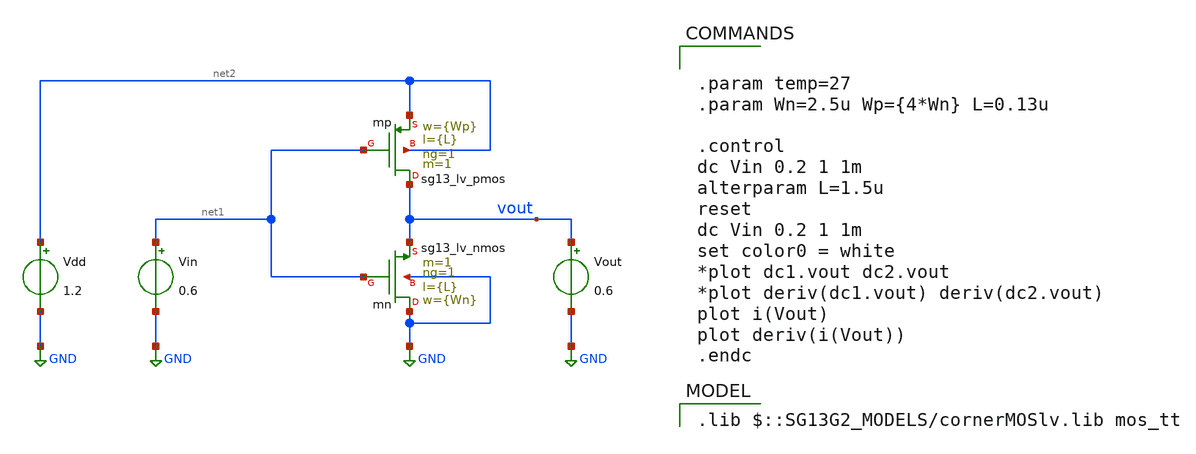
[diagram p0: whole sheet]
** sch_path: 5_Design/3_Real_circuits/sandbox_boris/tb_inv_gain.sch
**.subckt tb_inv_gain
Xmn GND net1 vout GND sg13_lv_nmos w={Wn} l={L} ng=1 m=1 mm_ok=1
Vin net1 GND 0.6
Xmp vout net1 net2 net2 sg13_lv_pmos w={Wp} l={L} ng=1 m=1 mm_ok=1
Vdd net2 GND 1.2
Vout vout GND 0.6
**** begin user architecture code
 .lib $::SG13G2_MODELS/cornerMOSlv.lib mos_tt



.param temp=27
.param Wn=2.5u Wp={4*Wn} L=0.13u

.control
dc Vin 0.2 1 1m
alterparam L=1.5u
reset
dc Vin 0.2 1 1m
set color0 = white
*plot dc1.vout dc2.vout
*plot deriv(dc1.vout) deriv(dc2.vout)
plot i(Vout)
plot deriv(i(Vout))
.endc


**** end user architecture code
**.ends
.GLOBAL GND
.end
